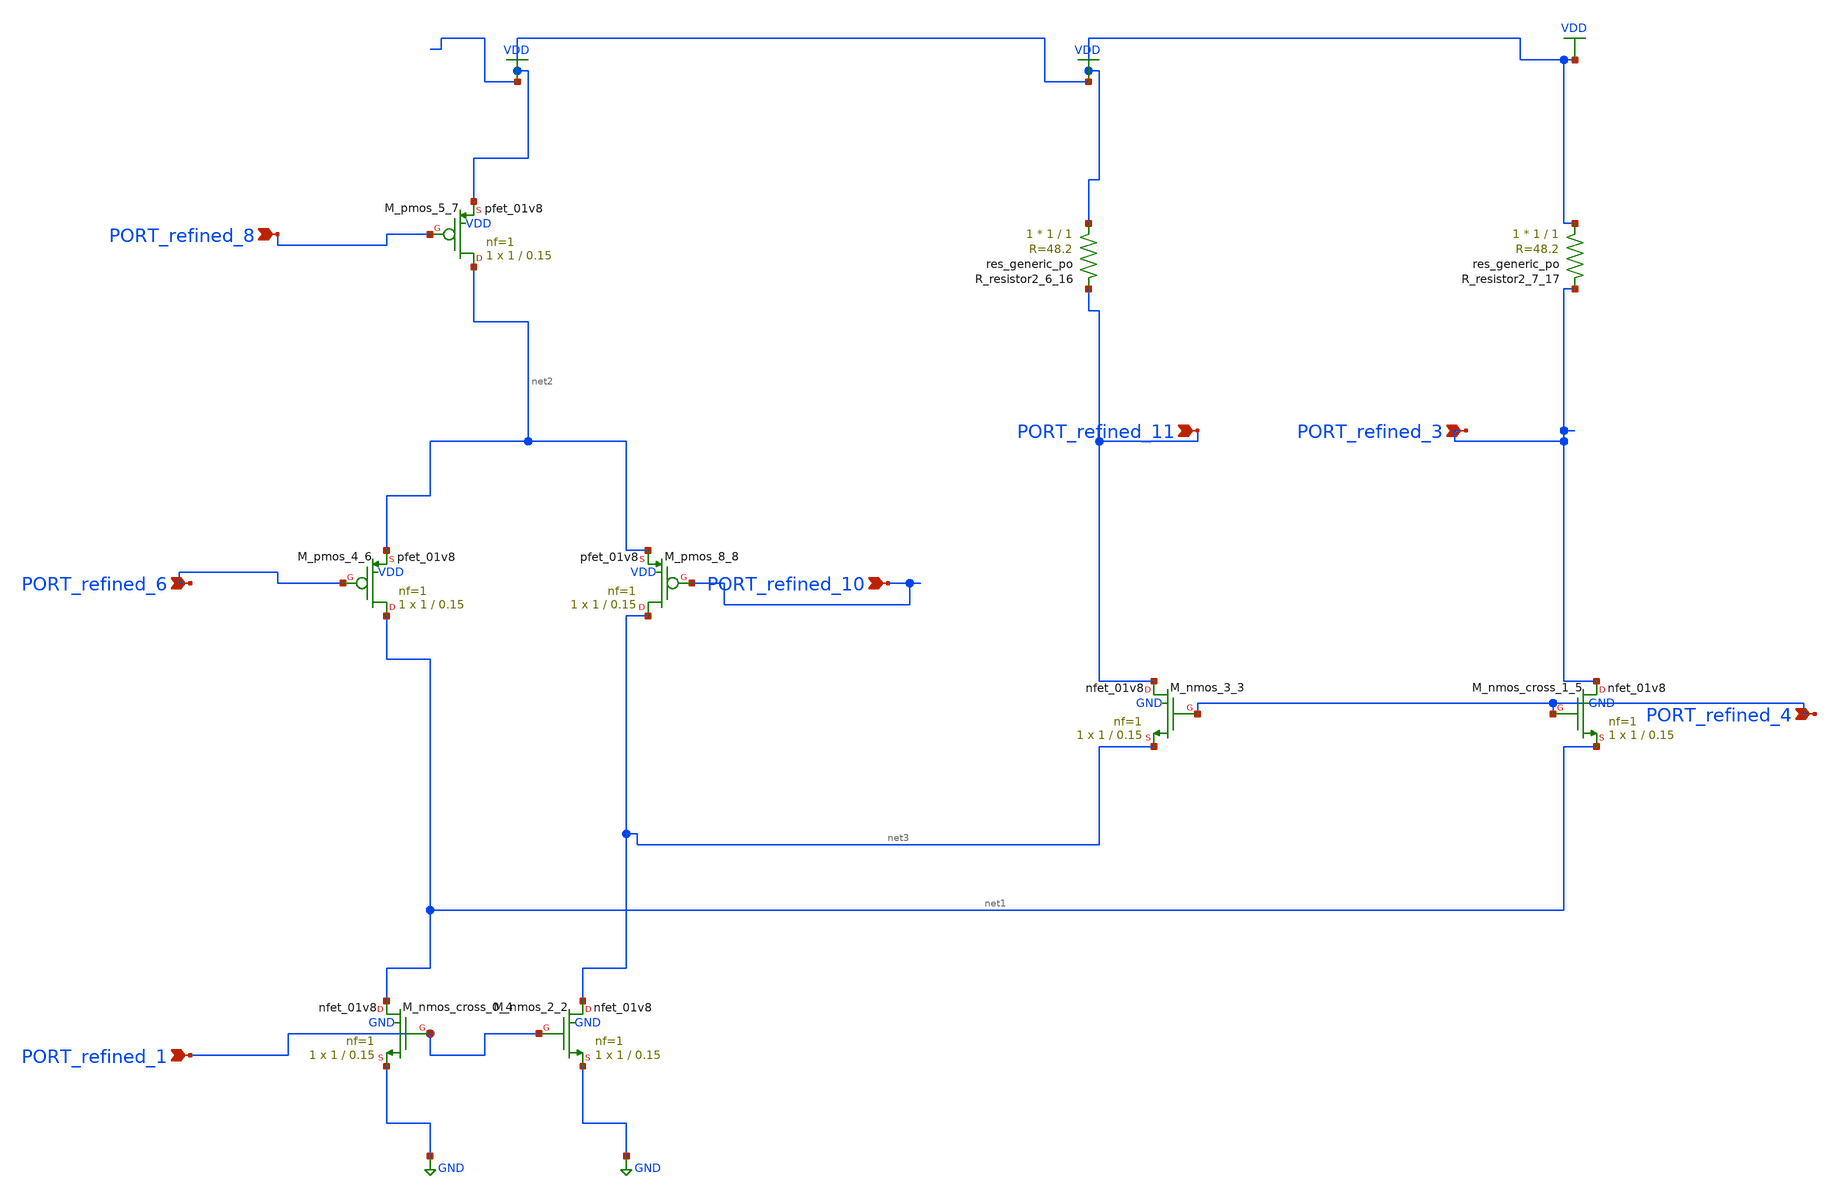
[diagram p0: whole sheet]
** sch_path: schematics/AMSNet/243.sch
**.subckt 243 PORT_refined_6 PORT_refined_3 PORT_refined_11 PORT_refined_1 PORT_refined_8
*+ PORT_refined_4 PORT_refined_10
*.ipin PORT_refined_6
*.ipin PORT_refined_3
*.ipin PORT_refined_11
*.ipin PORT_refined_1
*.ipin PORT_refined_8
*.ipin PORT_refined_4
*.ipin PORT_refined_10
XM_nmos_2_2 net3 PORT_refined_1 GND GND sky130_fd_pr__nfet_01v8 L=0.15 W=1 nf=1 ad='int((1 + 1)/2) * 1 / 1 * 0.29'
+ as='int((1 + 2)/2) * 1 / 1 * 0.29' pd='2*int((1 + 1)/2) * (1 / 1 + 0.29)' ps='2*int((1 + 2)/2) * (1 / 1 + 0.29)'
+ nrd='0.29 / 1 ' nrs='0.29 / 1 ' sa=0 sb=0 sd=0 mult=1 m=1
XM_nmos_3_3 PORT_refined_11 PORT_refined_4 net3 GND sky130_fd_pr__nfet_01v8 L=0.15 W=1 nf=1 ad='int((1 + 1)/2) * 1 / 1 * 0.29'
+ as='int((1 + 2)/2) * 1 / 1 * 0.29' pd='2*int((1 + 1)/2) * (1 / 1 + 0.29)' ps='2*int((1 + 2)/2) * (1 / 1 + 0.29)'
+ nrd='0.29 / 1 ' nrs='0.29 / 1 ' sa=0 sb=0 sd=0 mult=1 m=1
XM_nmos_cross_0_4 net1 PORT_refined_1 GND GND sky130_fd_pr__nfet_01v8 L=0.15 W=1 nf=1 ad='int((1 + 1)/2) * 1 / 1 * 0.29'
+ as='int((1 + 2)/2) * 1 / 1 * 0.29' pd='2*int((1 + 1)/2) * (1 / 1 + 0.29)' ps='2*int((1 + 2)/2) * (1 / 1 + 0.29)'
+ nrd='0.29 / 1 ' nrs='0.29 / 1 ' sa=0 sb=0 sd=0 mult=1 m=1
XM_nmos_cross_1_5 PORT_refined_3 PORT_refined_4 net1 GND sky130_fd_pr__nfet_01v8 L=0.15 W=1 nf=1 ad='int((1 + 1)/2) * 1 / 1 * 0.29'
+ as='int((1 + 2)/2) * 1 / 1 * 0.29' pd='2*int((1 + 1)/2) * (1 / 1 + 0.29)' ps='2*int((1 + 2)/2) * (1 / 1 + 0.29)'
+ nrd='0.29 / 1 ' nrs='0.29 / 1 ' sa=0 sb=0 sd=0 mult=1 m=1
XM_pmos_4_6 net1 PORT_refined_6 net2 VDD sky130_fd_pr__pfet_01v8 L=0.15 W=1 nf=1 ad='int((1 + 1)/2) * 1 / 1 * 0.29'
+ as='int((1 + 2)/2) * 1 / 1 * 0.29' pd='2*int((1 + 1)/2) * (1 / 1 + 0.29)' ps='2*int((1 + 2)/2) * (1 / 1 + 0.29)'
+ nrd='0.29 / 1 ' nrs='0.29 / 1 ' sa=0 sb=0 sd=0 mult=1 m=1
XM_pmos_5_7 net2 PORT_refined_8 VDD VDD sky130_fd_pr__pfet_01v8 L=0.15 W=1 nf=1 ad='int((1 + 1)/2) * 1 / 1 * 0.29'
+ as='int((1 + 2)/2) * 1 / 1 * 0.29' pd='2*int((1 + 1)/2) * (1 / 1 + 0.29)' ps='2*int((1 + 2)/2) * (1 / 1 + 0.29)'
+ nrd='0.29 / 1 ' nrs='0.29 / 1 ' sa=0 sb=0 sd=0 mult=1 m=1
XM_pmos_8_8 net3 PORT_refined_10 net2 VDD sky130_fd_pr__pfet_01v8 L=0.15 W=1 nf=1 ad='int((1 + 1)/2) * 1 / 1 * 0.29'
+ as='int((1 + 2)/2) * 1 / 1 * 0.29' pd='2*int((1 + 1)/2) * (1 / 1 + 0.29)' ps='2*int((1 + 2)/2) * (1 / 1 + 0.29)'
+ nrd='0.29 / 1 ' nrs='0.29 / 1 ' sa=0 sb=0 sd=0 mult=1 m=1
XR_resistor2_6_16 VDD PORT_refined_11 sky130_fd_pr__res_generic_po W=1 L=1 m=1
XR_resistor2_7_17 VDD PORT_refined_3 sky130_fd_pr__res_generic_po W=1 L=1 m=1
**.ends
.GLOBAL GND
.GLOBAL VDD
.end
